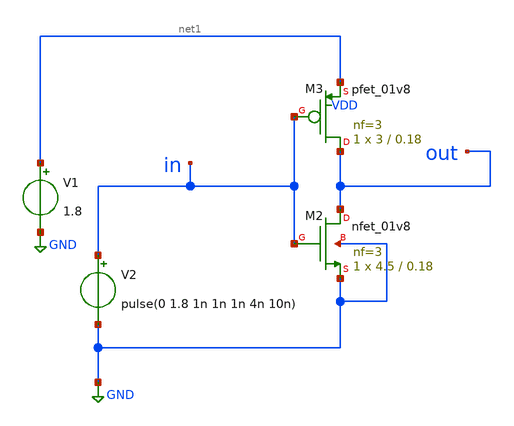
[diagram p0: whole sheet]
** sch_path: Week 0/xschem/Test_01.sch
**.subckt Test_01
XM2 out in GND GND sky130_fd_pr__nfet_01v8 L=0.18 W=4.5 nf=3 ad='int((nf+1)/2) * W/nf * 0.29' as='int((nf+2)/2) * W/nf * 0.29'
+ pd='2*int((nf+1)/2) * (W/nf + 0.29)' ps='2*int((nf+2)/2) * (W/nf + 0.29)' nrd='0.29 / W' nrs='0.29 / W'
+ sa=0 sb=0 sd=0 mult=1 m=1
XM3 out in net1 VDD sky130_fd_pr__pfet_01v8 L=0.18 W=3 nf=3 ad='int((nf+1)/2) * W/nf * 0.29' as='int((nf+2)/2) * W/nf * 0.29'
+ pd='2*int((nf+1)/2) * (W/nf + 0.29)' ps='2*int((nf+2)/2) * (W/nf + 0.29)' nrd='0.29 / W' nrs='0.29 / W'
+ sa=0 sb=0 sd=0 mult=1 m=1
V1 net1 GND 1.8
V2 in GND pulse(0 1.8 1n 1n 1n 4n 10n)
**.ends
.GLOBAL GND
**** begin user architecture code


.lib /usr/local/share/pdk/sky130A/libs.tech/ngspice/sky130.lib.spice tt
.control
	save all
	tran 1n 1u
	plot v(in) v(out)
.endc

**** end user architecture code
.end
